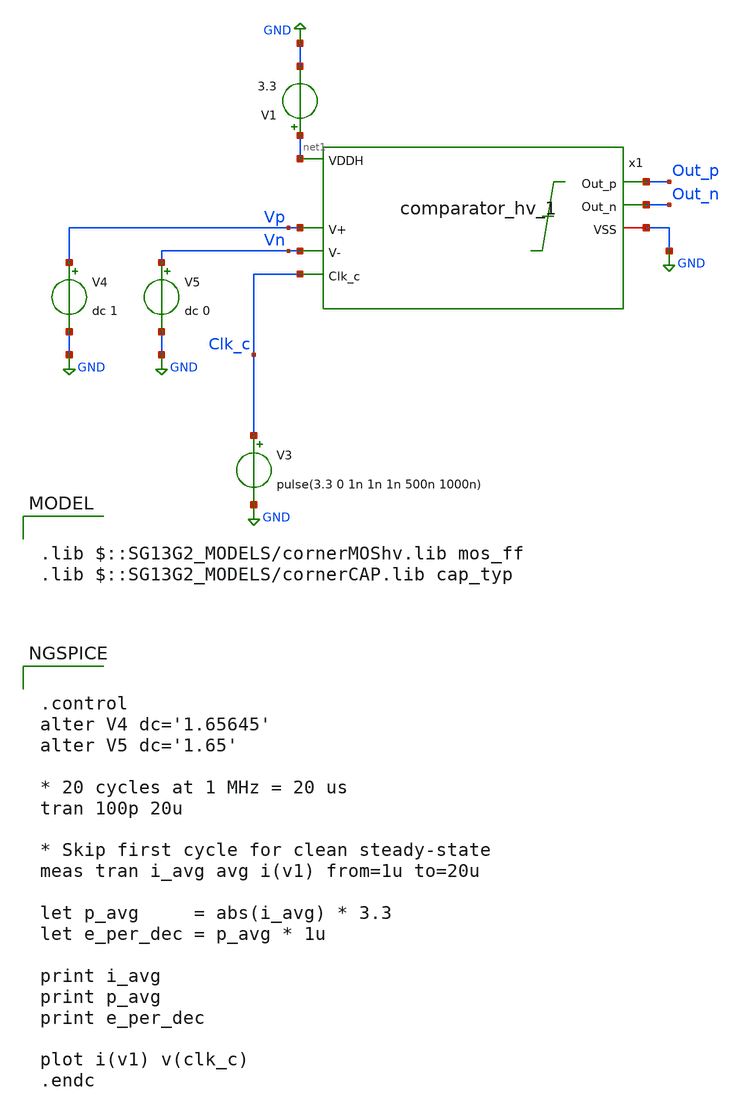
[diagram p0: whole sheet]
** sch_path: sar_adc/xschem/blocks/comparator/comparator_hv_tb.sch
**.subckt comparator_hv_tb
V3 Clk_c GND pulse(3.3 0 1n 1n 1n 500n 1000n)
V4 Vp GND dc 1
V5 Vn GND dc 0
V1 net1 GND 3.3
x1 net1 Vp Vn Out_p Out_n GND Clk_c comparator_hv_1
**** begin user architecture code

.lib $::SG13G2_MODELS/cornerMOShv.lib mos_ff
.lib $::SG13G2_MODELS/cornerCAP.lib cap_typ



.control
alter V4 dc='1.65645'
alter V5 dc='1.65'

* 20 cycles at 1 MHz = 20 us
tran 100p 20u

* Skip first cycle for clean steady-state
meas tran i_avg avg i(v1) from=1u to=20u

let p_avg     = abs(i_avg) * 3.3
let e_per_dec = p_avg * 1u

print i_avg
print p_avg
print e_per_dec

plot i(v1) v(clk_c)
.endc


**** end user architecture code
**.ends
.GLOBAL GND
.end
